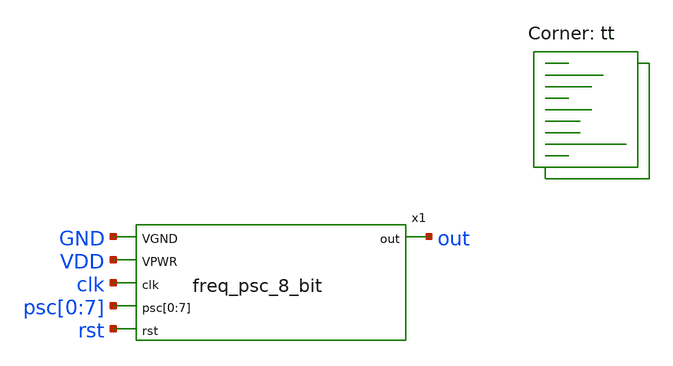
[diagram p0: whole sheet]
** sch_path: xschem/freq_psc_8_bit-tb.sch
**.subckt freq_psc_8_bit-tb
x1 GND VDD clk out psc[0] psc[1] psc[2] psc[3] psc[4] psc[5] psc[6] psc[7] rst freq_psc_8_bit
**** begin user architecture code



  .include ~/sky130_projects/sky130_its_biomedical_chip_research_2024/spice/freq_psc_8_bit.spice
  .param max_freq=8e6 period={1/max_freq} time_high={period/2}
  .param delay_vin1={time_high} delay_vin2={time_high*1.5}

  .option wnflag=1
  .option safecurrents

  Vvdd VDD GND dc 1.8
  *Vrst rst GND pulse(0 1.8 {delay_vin1*20} 1p 1p {time_high*20} {period*50})
  Vrst rst GND dc 0
  Vin1 clk GND pulse(0 1.8 {delay_vin1} 1p 1p {time_high} {period})

  Vpsc0  psc[0] gnd dc 1.8
  Vpsc1  psc[1] gnd dc 1.8
  Vpsc2  psc[2] gnd dc 1.8
  Vpsc3  psc[3] gnd dc 0
  Vpsc4  psc[4] gnd dc 0
  Vpsc5  psc[5] gnd dc 0
  Vpsc6  psc[6] gnd dc 0
  Vpsc7  psc[7] gnd dc 0

  .control
     reset
     save out clk psc[0] psc[1] psc[2] psc[3] psc[4] psc[5]
     +psc[6] psc[7] rst
     tran 0.01n 2u uic
     remzerovec
     write freq_psc_8_bit-tb.raw
    quit 0
  .endc



 .lib $::SKYWATER_MODELS/sky130.lib.spice tt
.include $::SKYWATER_STDCELLS/sky130_fd_sc_hd.spice
.include $::SKYWATER_STDCELLS/sky130_ef_sc_hd__decap_12.spice
.include $::SKYWATER_STDCELLS/sky130_ef_sc_hd__fill_4.spice
.include $::SKYWATER_STDCELLS/sky130_ef_sc_hd__fill_8.spice
.include $::SKYWATER_STDCELLS/sky130_ef_sc_hd__fill_12.spice
.param mc_mm_switch = 0
.param mc_pr_switch = 0

**** end user architecture code
**.ends
.end
